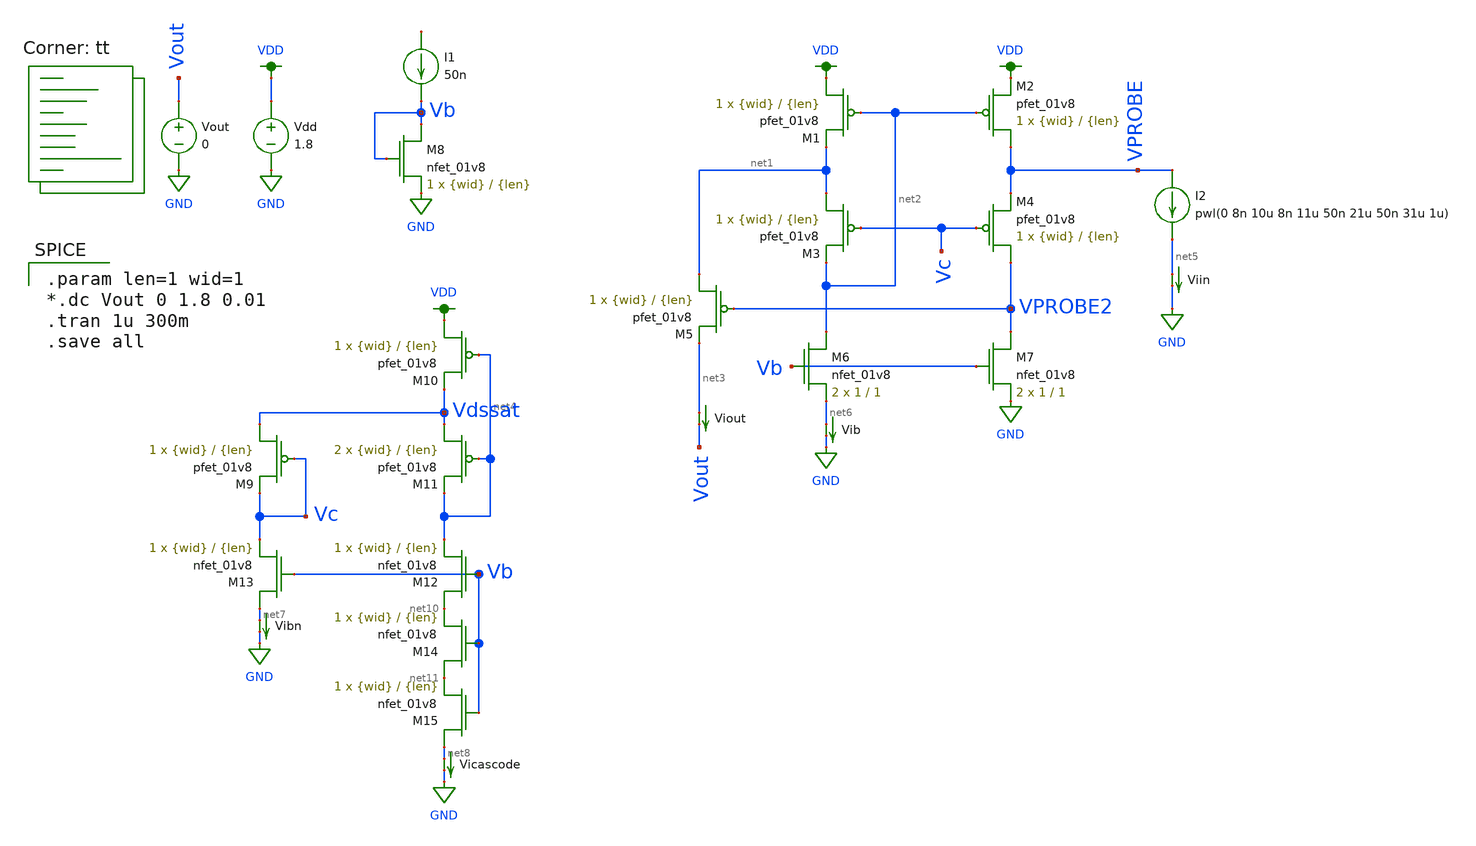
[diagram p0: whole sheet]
** sch_path: mp3/Reference Designs/mirror_tb.sch
**.subckt mirror_tb
XM1 VDD net2 net1 VDD sky130_fd_pr__pfet_01v8 L={len} W={wid} nf=1 ad='int((nf+1)/2) * W/nf * 0.29' as='int((nf+2)/2) * W/nf * 0.29'
+ pd='2*int((nf+1)/2) * (W/nf + 0.29)' ps='2*int((nf+2)/2) * (W/nf + 0.29)' nrd='0.29 / W' nrs='0.29 / W'
+ sa=0 sb=0 sd=0 mult=1 m=1
XM2 VPROBE net2 VDD VDD sky130_fd_pr__pfet_01v8 L={len} W={wid} nf=1 ad='int((nf+1)/2) * W/nf * 0.29'
+ as='int((nf+2)/2) * W/nf * 0.29' pd='2*int((nf+1)/2) * (W/nf + 0.29)' ps='2*int((nf+2)/2) * (W/nf + 0.29)'
+ nrd='0.29 / W' nrs='0.29 / W' sa=0 sb=0 sd=0 mult=1 m=1
XM3 net1 Vc net2 VDD sky130_fd_pr__pfet_01v8 L={len} W={wid} nf=1 ad='int((nf+1)/2) * W/nf * 0.29' as='int((nf+2)/2) * W/nf * 0.29'
+ pd='2*int((nf+1)/2) * (W/nf + 0.29)' ps='2*int((nf+2)/2) * (W/nf + 0.29)' nrd='0.29 / W' nrs='0.29 / W'
+ sa=0 sb=0 sd=0 mult=1 m=1
XM4 VPROBE2 Vc VPROBE VDD sky130_fd_pr__pfet_01v8 L={len} W={wid} nf=1 ad='int((nf+1)/2) * W/nf * 0.29'
+ as='int((nf+2)/2) * W/nf * 0.29' pd='2*int((nf+1)/2) * (W/nf + 0.29)' ps='2*int((nf+2)/2) * (W/nf + 0.29)'
+ nrd='0.29 / W' nrs='0.29 / W' sa=0 sb=0 sd=0 mult=1 m=1
XM5 net1 VPROBE2 net3 VDD sky130_fd_pr__pfet_01v8 L={len} W={wid} nf=1 ad='int((nf+1)/2) * W/nf * 0.29'
+ as='int((nf+2)/2) * W/nf * 0.29' pd='2*int((nf+1)/2) * (W/nf + 0.29)' ps='2*int((nf+2)/2) * (W/nf + 0.29)'
+ nrd='0.29 / W' nrs='0.29 / W' sa=0 sb=0 sd=0 mult=1 m=1
XM6 net2 Vb net6 GND sky130_fd_pr__nfet_01v8 L=1 W=1 nf=1 ad='int((nf+1)/2) * W/nf * 0.29' as='int((nf+2)/2) * W/nf * 0.29'
+ pd='2*int((nf+1)/2) * (W/nf + 0.29)' ps='2*int((nf+2)/2) * (W/nf + 0.29)' nrd='0.29 / W' nrs='0.29 / W'
+ sa=0 sb=0 sd=0 mult=2 m=2
XM7 VPROBE2 Vb GND GND sky130_fd_pr__nfet_01v8 L=1 W=1 nf=1 ad='int((nf+1)/2) * W/nf * 0.29' as='int((nf+2)/2) * W/nf * 0.29'
+ pd='2*int((nf+1)/2) * (W/nf + 0.29)' ps='2*int((nf+2)/2) * (W/nf + 0.29)' nrd='0.29 / W' nrs='0.29 / W'
+ sa=0 sb=0 sd=0 mult=2 m=2
XM8 Vb Vb GND GND sky130_fd_pr__nfet_01v8 L={len} W={wid} nf=1 ad='int((nf+1)/2) * W/nf * 0.29' as='int((nf+2)/2) * W/nf * 0.29'
+ pd='2*int((nf+1)/2) * (W/nf + 0.29)' ps='2*int((nf+2)/2) * (W/nf + 0.29)' nrd='0.29 / W' nrs='0.29 / W'
+ sa=0 sb=0 sd=0 mult=1 m=1
I1 net9 Vb 50n
I2 VPROBE net5 pwl(0 8n 10u 8n 11u 50n 21u 50n 31u 1u)
Viout net3 Vout 0
.save i(viout)
XM9 Vdssat Vc Vc VDD sky130_fd_pr__pfet_01v8 L={len} W={wid} nf=1 ad='int((nf+1)/2) * W/nf * 0.29' as='int((nf+2)/2) * W/nf * 0.29'
+ pd='2*int((nf+1)/2) * (W/nf + 0.29)' ps='2*int((nf+2)/2) * (W/nf + 0.29)' nrd='0.29 / W' nrs='0.29 / W'
+ sa=0 sb=0 sd=0 mult=1 m=1
XM10 VDD net4 Vdssat VDD sky130_fd_pr__pfet_01v8 L={len} W={wid} nf=1 ad='int((nf+1)/2) * W/nf * 0.29'
+ as='int((nf+2)/2) * W/nf * 0.29' pd='2*int((nf+1)/2) * (W/nf + 0.29)' ps='2*int((nf+2)/2) * (W/nf + 0.29)'
+ nrd='0.29 / W' nrs='0.29 / W' sa=0 sb=0 sd=0 mult=1 m=1
XM11 Vdssat net4 net4 VDD sky130_fd_pr__pfet_01v8 L={len} W={wid} nf=1 ad='int((nf+1)/2) * W/nf * 0.29'
+ as='int((nf+2)/2) * W/nf * 0.29' pd='2*int((nf+1)/2) * (W/nf + 0.29)' ps='2*int((nf+2)/2) * (W/nf + 0.29)'
+ nrd='0.29 / W' nrs='0.29 / W' sa=0 sb=0 sd=0 mult=2 m=2
XM13 net7 Vb Vc GND sky130_fd_pr__nfet_01v8 L={len} W={wid} nf=1 ad='int((nf+1)/2) * W/nf * 0.29' as='int((nf+2)/2) * W/nf * 0.29'
+ pd='2*int((nf+1)/2) * (W/nf + 0.29)' ps='2*int((nf+2)/2) * (W/nf + 0.29)' nrd='0.29 / W' nrs='0.29 / W'
+ sa=0 sb=0 sd=0 mult=1 m=1
Vdd VDD GND 1.8
Viin net5 GND 0
.save i(viin)
Vib net6 GND 0
.save i(vib)
Vibn net7 GND 0
.save i(vibn)
Vout Vout GND 0
XM12 net10 Vb net4 GND sky130_fd_pr__nfet_01v8 L={len} W={wid} nf=1 ad='int((nf+1)/2) * W/nf * 0.29'
+ as='int((nf+2)/2) * W/nf * 0.29' pd='2*int((nf+1)/2) * (W/nf + 0.29)' ps='2*int((nf+2)/2) * (W/nf + 0.29)'
+ nrd='0.29 / W' nrs='0.29 / W' sa=0 sb=0 sd=0 mult=1 m=1
XM14 net11 Vb net10 GND sky130_fd_pr__nfet_01v8 L={len} W={wid} nf=1 ad='int((nf+1)/2) * W/nf * 0.29'
+ as='int((nf+2)/2) * W/nf * 0.29' pd='2*int((nf+1)/2) * (W/nf + 0.29)' ps='2*int((nf+2)/2) * (W/nf + 0.29)'
+ nrd='0.29 / W' nrs='0.29 / W' sa=0 sb=0 sd=0 mult=1 m=1
XM15 net8 Vb net11 GND sky130_fd_pr__nfet_01v8 L={len} W={wid} nf=1 ad='int((nf+1)/2) * W/nf * 0.29'
+ as='int((nf+2)/2) * W/nf * 0.29' pd='2*int((nf+1)/2) * (W/nf + 0.29)' ps='2*int((nf+2)/2) * (W/nf + 0.29)'
+ nrd='0.29 / W' nrs='0.29 / W' sa=0 sb=0 sd=0 mult=1 m=1
Vicascode net8 GND 0
.save i(vicascode)
**** begin user architecture code

.param len=1 wid=1
*.dc Vout 0 1.8 0.01
.tran 1u 300m
.save all


.lib $::SKYWATER_MODELS/sky130.lib.spice tt
**** end user architecture code
**.ends
.GLOBAL GND
.GLOBAL VDD
.end
